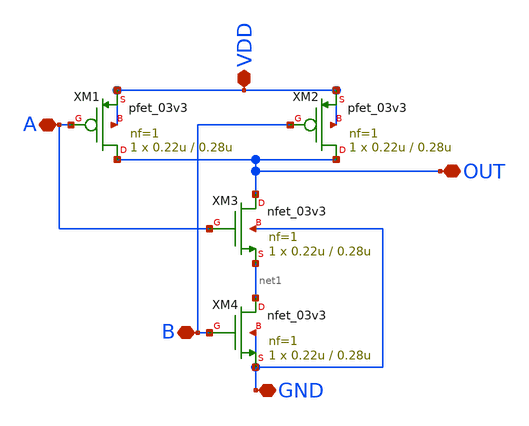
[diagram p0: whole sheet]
** sch_path: xschem/NAND.sch
**.subckt NAND OUT GND VDD A B
*.iopin OUT
*.iopin GND
*.iopin VDD
*.iopin A
*.iopin B
XM1 OUT A VDD VDD pfet_03v3 L=0.28u W=0.22u nf=1 ad='int((nf+1)/2) * W/nf * 0.18u' as='int((nf+2)/2) * W/nf * 0.18u'
+ pd='2*int((nf+1)/2) * (W/nf + 0.18u)' ps='2*int((nf+2)/2) * (W/nf + 0.18u)' nrd='0.18u / W' nrs='0.18u / W'
+ sa=0 sb=0 sd=0 m=1
XM2 OUT B VDD VDD pfet_03v3 L=0.28u W=0.22u nf=1 ad='int((nf+1)/2) * W/nf * 0.18u' as='int((nf+2)/2) * W/nf * 0.18u'
+ pd='2*int((nf+1)/2) * (W/nf + 0.18u)' ps='2*int((nf+2)/2) * (W/nf + 0.18u)' nrd='0.18u / W' nrs='0.18u / W'
+ sa=0 sb=0 sd=0 m=1
XM3 OUT A net1 GND nfet_03v3 L=0.28u W=0.22u nf=1 ad='int((nf+1)/2) * W/nf * 0.18u' as='int((nf+2)/2) * W/nf * 0.18u'
+ pd='2*int((nf+1)/2) * (W/nf + 0.18u)' ps='2*int((nf+2)/2) * (W/nf + 0.18u)' nrd='0.18u / W' nrs='0.18u / W'
+ sa=0 sb=0 sd=0 m=1
XM4 net1 B GND GND nfet_03v3 L=0.28u W=0.22u nf=1 ad='int((nf+1)/2) * W/nf * 0.18u' as='int((nf+2)/2) * W/nf * 0.18u'
+ pd='2*int((nf+1)/2) * (W/nf + 0.18u)' ps='2*int((nf+2)/2) * (W/nf + 0.18u)' nrd='0.18u / W' nrs='0.18u / W'
+ sa=0 sb=0 sd=0 m=1
**.ends
.end
